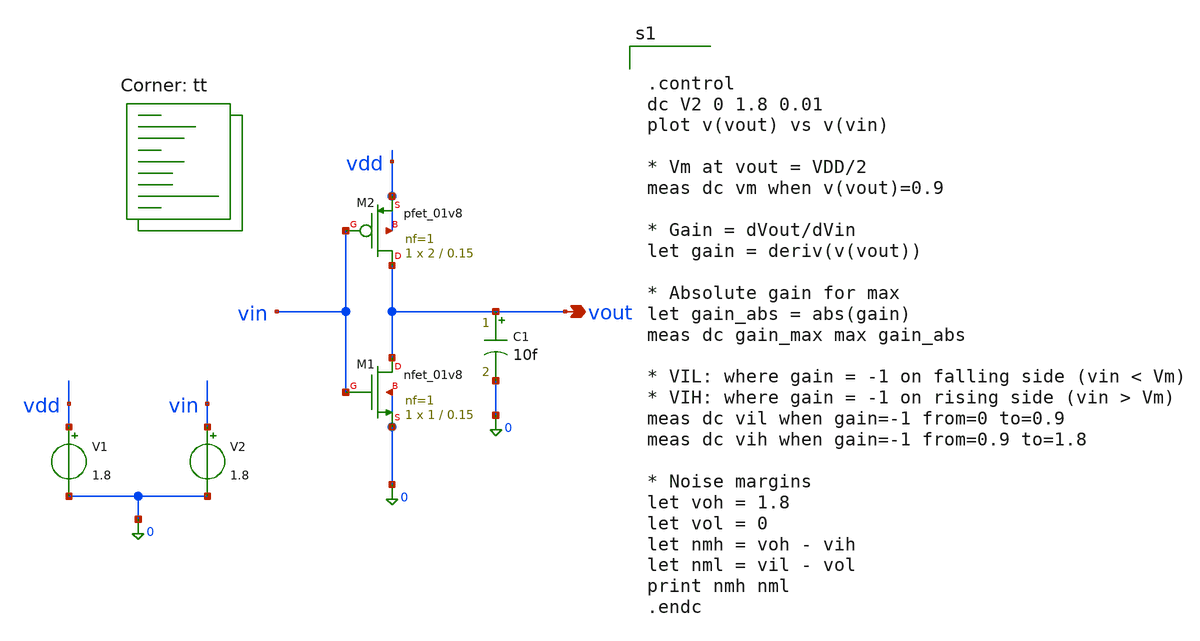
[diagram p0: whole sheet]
** sch_path: 02_simulation/dc/inverter_dc.sch
**.subckt inverter_dc vout
*.opin vout
XM1 vout vin 0 0 sky130_fd_pr__nfet_01v8 L=0.15 W=1 nf=1 ad='int((1 + 1)/2) * 1 / 1 * 0.29' as='int((1 + 2)/2) * 1 / 1 * 0.29'
+ pd='2*int((1 + 1)/2) * (1 / 1 + 0.29)' ps='2*int((1 + 2)/2) * (1 / 1 + 0.29)' nrd='0.29 / 1 ' nrs='0.29 / 1 '
+ sa=0 sb=0 sd=0 mult=1 m=1
XM2 vout vin vdd vdd sky130_fd_pr__pfet_01v8 L=0.15 W=2 nf=1 ad='int((1 + 1)/2) * 2 / 1 * 0.29' as='int((1 + 2)/2) * 2 / 1 * 0.29'
+ pd='2*int((1 + 1)/2) * (2 / 1 + 0.29)' ps='2*int((1 + 2)/2) * (2 / 1 + 0.29)' nrd='0.29 / 2 ' nrs='0.29 / 2 '
+ sa=0 sb=0 sd=0 mult=1 m=1
V1 vdd 0 1.8
V2 vin 0 1.8
C1 vout 0 10f m=1
**** begin user architecture code
.lib $::SKYWATER_MODELS/sky130.lib.spice tt


.control
dc V2 0 1.8 0.01
plot v(vout) vs v(vin)

* Vm at vout = VDD/2
meas dc vm when v(vout)=0.9

* Gain = dVout/dVin
let gain = deriv(v(vout))

* Absolute gain for max
let gain_abs = abs(gain)
meas dc gain_max max gain_abs

* VIL: where gain = -1 on falling side (vin < Vm)
* VIH: where gain = -1 on rising side (vin > Vm)
meas dc vil when gain=-1 from=0 to=0.9
meas dc vih when gain=-1 from=0.9 to=1.8

* Noise margins
let voh = 1.8
let vol = 0
let nmh = voh - vih
let nml = vil - vol
print nmh nml
.endc


**** end user architecture code
**.ends
.end
